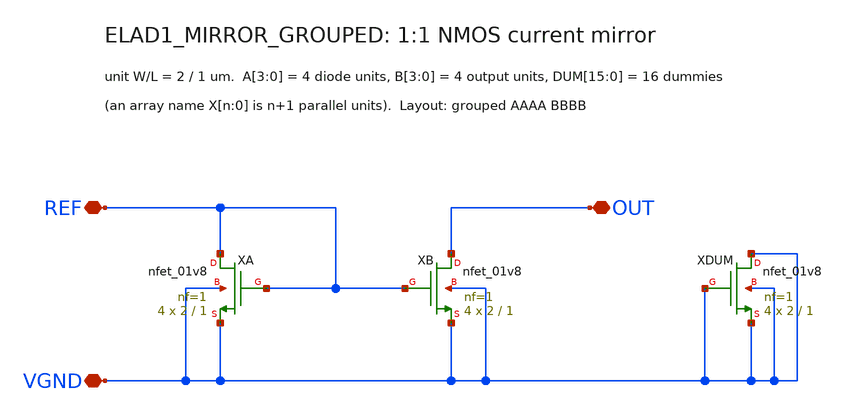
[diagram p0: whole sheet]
** sch_path: cells/ELAD1_MIRROR_GROUPED/schematic/ELAD1_MIRROR_GROUPED.sch
**.subckt ELAD1_MIRROR_GROUPED REF OUT VGND
*.iopin REF
*.iopin OUT
*.iopin VGND
XXA REF REF VGND VGND sky130_fd_pr__nfet_01v8 L=1 W=2 nf=1 ad='int((1 + 1)/2) * 2 / 1 * 0.29' as='int((1 + 2)/2) * 2 / 1 * 0.29'
+ pd='2*int((1 + 1)/2) * (2 / 1 + 0.29)' ps='2*int((1 + 2)/2) * (2 / 1 + 0.29)' nrd='0.29 / 2 ' nrs='0.29 / 2 '
+ sa=0 sb=0 sd=0 mult=4 m=4
XXB OUT REF VGND VGND sky130_fd_pr__nfet_01v8 L=1 W=2 nf=1 ad='int((1 + 1)/2) * 2 / 1 * 0.29' as='int((1 + 2)/2) * 2 / 1 * 0.29'
+ pd='2*int((1 + 1)/2) * (2 / 1 + 0.29)' ps='2*int((1 + 2)/2) * (2 / 1 + 0.29)' nrd='0.29 / 2 ' nrs='0.29 / 2 '
+ sa=0 sb=0 sd=0 mult=4 m=4
XXDUM VGND VGND VGND VGND sky130_fd_pr__nfet_01v8 L=1 W=2 nf=1 ad='int((1 + 1)/2) * 2 / 1 * 0.29' as='int((1 + 2)/2) * 2 / 1 * 0.29'
+ pd='2*int((1 + 1)/2) * (2 / 1 + 0.29)' ps='2*int((1 + 2)/2) * (2 / 1 + 0.29)' nrd='0.29 / 2 ' nrs='0.29 / 2 '
+ sa=0 sb=0 sd=0 mult=4 m=4
**.ends
.end
